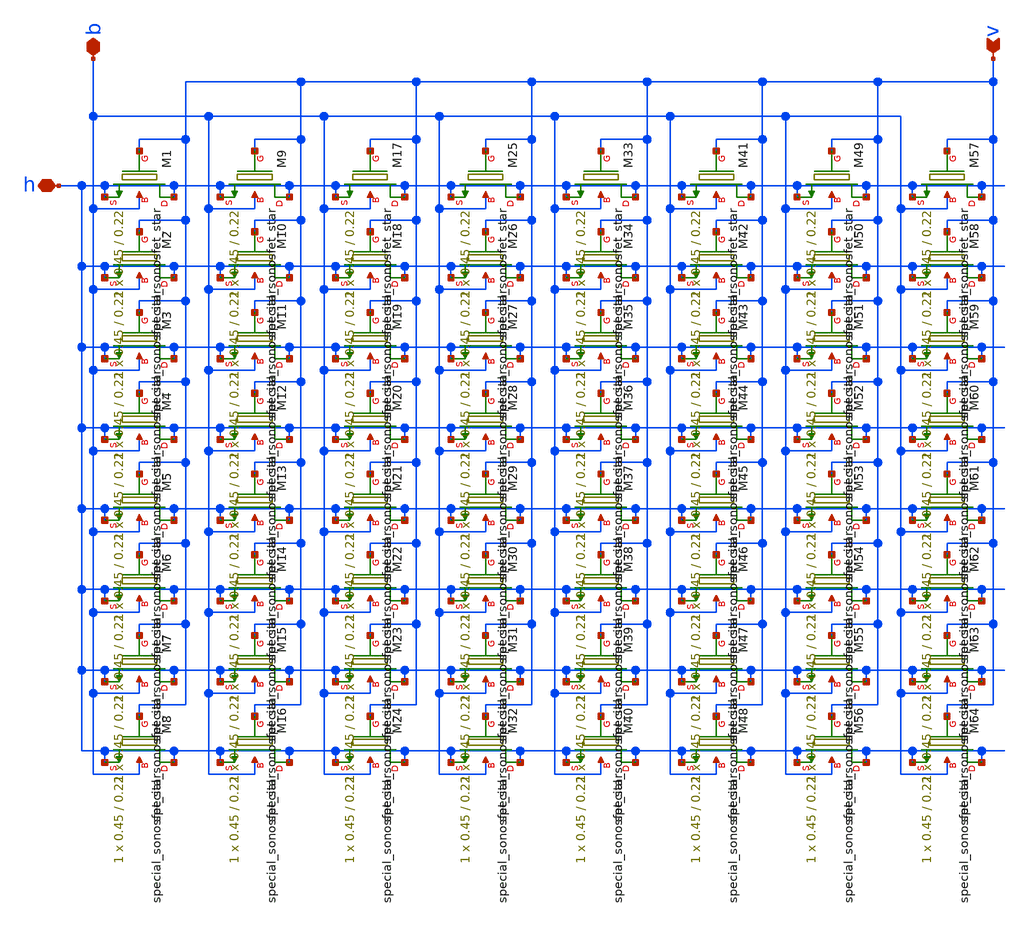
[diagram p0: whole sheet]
** sch_path: xschem/sonos_array_small_8x8.sch
**.subckt sonos_array_small_8x8 v b h
*.ipin v
*.iopin b
*.iopin h
XM1 h v h b sky130_fd_bs__special_sonosfet_star L=0.22 W=0.45 m=1
XM2 h v h b sky130_fd_bs__special_sonosfet_star L=0.22 W=0.45 m=1
XM3 h v h b sky130_fd_bs__special_sonosfet_star L=0.22 W=0.45 m=1
XM4 h v h b sky130_fd_bs__special_sonosfet_star L=0.22 W=0.45 m=1
XM5 h v h b sky130_fd_bs__special_sonosfet_star L=0.22 W=0.45 m=1
XM6 h v h b sky130_fd_bs__special_sonosfet_star L=0.22 W=0.45 m=1
XM7 h v h b sky130_fd_bs__special_sonosfet_star L=0.22 W=0.45 m=1
XM8 h v h b sky130_fd_bs__special_sonosfet_star L=0.22 W=0.45 m=1
XM9 h v h b sky130_fd_bs__special_sonosfet_star L=0.22 W=0.45 m=1
XM10 h v h b sky130_fd_bs__special_sonosfet_star L=0.22 W=0.45 m=1
XM11 h v h b sky130_fd_bs__special_sonosfet_star L=0.22 W=0.45 m=1
XM12 h v h b sky130_fd_bs__special_sonosfet_star L=0.22 W=0.45 m=1
XM13 h v h b sky130_fd_bs__special_sonosfet_star L=0.22 W=0.45 m=1
XM14 h v h b sky130_fd_bs__special_sonosfet_star L=0.22 W=0.45 m=1
XM15 h v h b sky130_fd_bs__special_sonosfet_star L=0.22 W=0.45 m=1
XM16 h v h b sky130_fd_bs__special_sonosfet_star L=0.22 W=0.45 m=1
XM17 h v h b sky130_fd_bs__special_sonosfet_star L=0.22 W=0.45 m=1
XM18 h v h b sky130_fd_bs__special_sonosfet_star L=0.22 W=0.45 m=1
XM19 h v h b sky130_fd_bs__special_sonosfet_star L=0.22 W=0.45 m=1
XM20 h v h b sky130_fd_bs__special_sonosfet_star L=0.22 W=0.45 m=1
XM21 h v h b sky130_fd_bs__special_sonosfet_star L=0.22 W=0.45 m=1
XM22 h v h b sky130_fd_bs__special_sonosfet_star L=0.22 W=0.45 m=1
XM23 h v h b sky130_fd_bs__special_sonosfet_star L=0.22 W=0.45 m=1
XM24 h v h b sky130_fd_bs__special_sonosfet_star L=0.22 W=0.45 m=1
XM25 h v h b sky130_fd_bs__special_sonosfet_star L=0.22 W=0.45 m=1
XM26 h v h b sky130_fd_bs__special_sonosfet_star L=0.22 W=0.45 m=1
XM27 h v h b sky130_fd_bs__special_sonosfet_star L=0.22 W=0.45 m=1
XM28 h v h b sky130_fd_bs__special_sonosfet_star L=0.22 W=0.45 m=1
XM29 h v h b sky130_fd_bs__special_sonosfet_star L=0.22 W=0.45 m=1
XM30 h v h b sky130_fd_bs__special_sonosfet_star L=0.22 W=0.45 m=1
XM31 h v h b sky130_fd_bs__special_sonosfet_star L=0.22 W=0.45 m=1
XM32 h v h b sky130_fd_bs__special_sonosfet_star L=0.22 W=0.45 m=1
XM33 h v h b sky130_fd_bs__special_sonosfet_star L=0.22 W=0.45 m=1
XM34 h v h b sky130_fd_bs__special_sonosfet_star L=0.22 W=0.45 m=1
XM35 h v h b sky130_fd_bs__special_sonosfet_star L=0.22 W=0.45 m=1
XM36 h v h b sky130_fd_bs__special_sonosfet_star L=0.22 W=0.45 m=1
XM37 h v h b sky130_fd_bs__special_sonosfet_star L=0.22 W=0.45 m=1
XM38 h v h b sky130_fd_bs__special_sonosfet_star L=0.22 W=0.45 m=1
XM39 h v h b sky130_fd_bs__special_sonosfet_star L=0.22 W=0.45 m=1
XM40 h v h b sky130_fd_bs__special_sonosfet_star L=0.22 W=0.45 m=1
XM41 h v h b sky130_fd_bs__special_sonosfet_star L=0.22 W=0.45 m=1
XM42 h v h b sky130_fd_bs__special_sonosfet_star L=0.22 W=0.45 m=1
XM43 h v h b sky130_fd_bs__special_sonosfet_star L=0.22 W=0.45 m=1
XM44 h v h b sky130_fd_bs__special_sonosfet_star L=0.22 W=0.45 m=1
XM45 h v h b sky130_fd_bs__special_sonosfet_star L=0.22 W=0.45 m=1
XM46 h v h b sky130_fd_bs__special_sonosfet_star L=0.22 W=0.45 m=1
XM47 h v h b sky130_fd_bs__special_sonosfet_star L=0.22 W=0.45 m=1
XM48 h v h b sky130_fd_bs__special_sonosfet_star L=0.22 W=0.45 m=1
XM49 h v h b sky130_fd_bs__special_sonosfet_star L=0.22 W=0.45 m=1
XM50 h v h b sky130_fd_bs__special_sonosfet_star L=0.22 W=0.45 m=1
XM51 h v h b sky130_fd_bs__special_sonosfet_star L=0.22 W=0.45 m=1
XM52 h v h b sky130_fd_bs__special_sonosfet_star L=0.22 W=0.45 m=1
XM53 h v h b sky130_fd_bs__special_sonosfet_star L=0.22 W=0.45 m=1
XM54 h v h b sky130_fd_bs__special_sonosfet_star L=0.22 W=0.45 m=1
XM55 h v h b sky130_fd_bs__special_sonosfet_star L=0.22 W=0.45 m=1
XM56 h v h b sky130_fd_bs__special_sonosfet_star L=0.22 W=0.45 m=1
XM57 h v h b sky130_fd_bs__special_sonosfet_star L=0.22 W=0.45 m=1
XM58 h v h b sky130_fd_bs__special_sonosfet_star L=0.22 W=0.45 m=1
XM59 h v h b sky130_fd_bs__special_sonosfet_star L=0.22 W=0.45 m=1
XM60 h v h b sky130_fd_bs__special_sonosfet_star L=0.22 W=0.45 m=1
XM61 h v h b sky130_fd_bs__special_sonosfet_star L=0.22 W=0.45 m=1
XM62 h v h b sky130_fd_bs__special_sonosfet_star L=0.22 W=0.45 m=1
XM63 h v h b sky130_fd_bs__special_sonosfet_star L=0.22 W=0.45 m=1
XM64 h v h b sky130_fd_bs__special_sonosfet_star L=0.22 W=0.45 m=1
**.ends
.end
